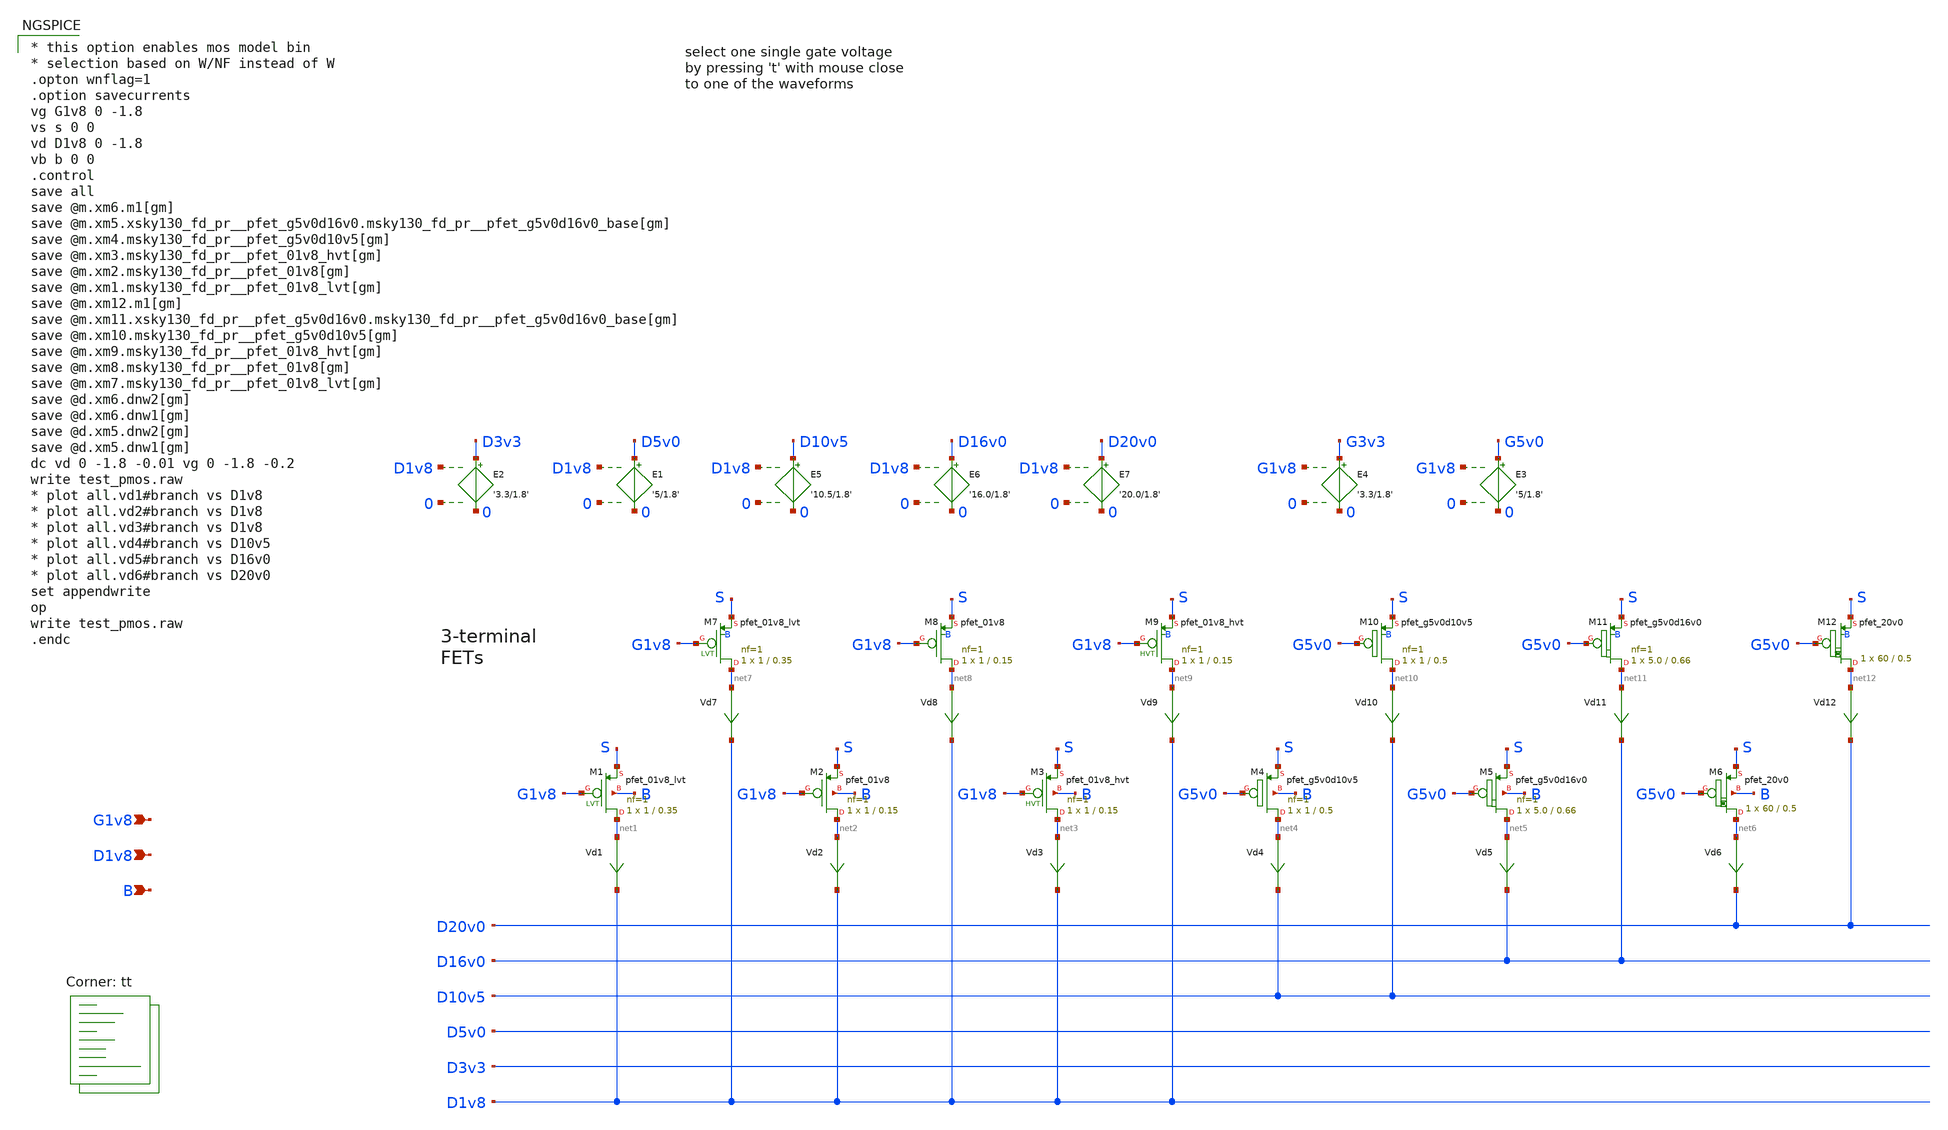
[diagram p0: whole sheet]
** sch_path: sky130A/xschem_libs/sky130_tests/test_pmos/schematic/test_pmos.sch
* Copyright 2021 Stefan Frederik Schippers
* Licensed under the Apache License, Version 2.0 (the "License");
* you may not use this file except in compliance with the License.
* You may obtain a copy of the License at
* https://www.apache.org/licenses/LICENSE-2.0
* Unless required by applicable law or agreed to in writing, software
* distributed under the License is distributed on an "AS IS" BASIS,
* WITHOUT WARRANTIES OR CONDITIONS OF ANY KIND, either express or implied.
* See the License for the specific language governing permissions and
* limitations under the License.
**.subckt test_pmos G1v8 D1v8 B
*.ipin G1v8
*.ipin D1v8
*.ipin B
Vd1 net1 D1v8 0
.save i(vd1)
Vd2 net2 D1v8 0
.save i(vd2)
E1 D5v0 0 D1v8 0 '5/1.8'
E2 D3v3 0 D1v8 0 '3.3/1.8'
E3 G5v0 0 G1v8 0 '5/1.8'
E4 G3v3 0 G1v8 0 '3.3/1.8'
E5 D10v5 0 D1v8 0 '10.5/1.8'
Vd3 net3 D1v8 0
.save i(vd3)
XM3 net3 G1v8 S B sky130_fd_pr__pfet_01v8_hvt L=0.15 W=1 nf=1 ad='int((1 + 1)/2) * 1 / 1 * 0.29' as='int((1 + 2)/2) * 1 / 1 * 0.29'
+ pd='2*int((1 + 1)/2) * (1 / 1 + 0.29)' ps='2*int((1 + 2)/2) * (1 / 1 + 0.29)' nrd='0.29 / 1 ' nrs='0.29 / 1 '
+ sa=0 sb=0 sd=0 mult=1 m=1
Vd4 net4 D10v5 0
.save i(vd4)
XM4 net4 G5v0 S B sky130_fd_pr__pfet_g5v0d10v5 L=0.5 W=1 nf=1 ad='int((1 + 1)/2) * 1 / 1 * 0.29' as='int((1 + 2)/2) * 1 / 1 * 0.29'
+ pd='2*int((1 + 1)/2) * (1 / 1 + 0.29)' ps='2*int((1 + 2)/2) * (1 / 1 + 0.29)' nrd='0.29 / 1 ' nrs='0.29 / 1 '
+ sa=0 sb=0 sd=0 mult=1 m=1
XM1 net1 G1v8 S B sky130_fd_pr__pfet_01v8_lvt L=0.35 W=1 nf=1 ad='int((1 + 1)/2) * 1 / 1 * 0.29' as='int((1 + 2)/2) * 1 / 1 * 0.29'
+ pd='2*int((1 + 1)/2) * (1 / 1 + 0.29)' ps='2*int((1 + 2)/2) * (1 / 1 + 0.29)' nrd='0.29 / 1 ' nrs='0.29 / 1 '
+ sa=0 sb=0 sd=0 mult=1 m=1
XM2 net2 G1v8 S B sky130_fd_pr__pfet_01v8 L=0.15 W=1 nf=1 ad='int((nf+1)/2) * W/nf * 0.29' as='int((nf+2)/2) * W/nf * 0.29'
+ pd='2*int((nf+1)/2) * (W/nf + 0.29)' ps='2*int((nf+2)/2) * (W/nf + 0.29)' nrd='0.29 / W' nrs='0.29 / W'
+ sa=0 sb=0 sd=0 mult=1 m=1
Vd5 net5 D16v0 0
.save i(vd5)
XM5 net5 G5v0 S B sky130_fd_pr__pfet_g5v0d16v0 L=0.66 W=5.0 nf=1 ad='int((nf+1)/2) * W/nf * 0.29' as='int((nf+2)/2) * W/nf * 0.29'
+ pd='2*int((nf+1)/2) * (W/nf + 0.29)' ps='2*int((nf+2)/2) * (W/nf + 0.29)' nrd='0.29 / W' nrs='0.29 / W'
+ sa=0 sb=0 sd=0 mult=1 m=1
E6 D16v0 0 D1v8 0 '16.0/1.8'
E7 D20v0 0 D1v8 0 '20.0/1.8'
XM6 net6 G5v0 S B sky130_fd_pr__pfet_20v0 L=0.5 W=60 m=1
Vd6 net6 D20v0 0
.save i(vd6)
Vd7 net7 D1v8 0
.save i(vd7)
Vd8 net8 D1v8 0
.save i(vd8)
Vd9 net9 D1v8 0
.save i(vd9)
XM9 net9 G1v8 S B sky130_fd_pr__pfet_01v8_hvt L=0.15 W=1 nf=1 ad='int((1 + 1)/2) * 1 / 1 * 0.29' as='int((1 + 2)/2) * 1 / 1 * 0.29'
+ pd='2*int((1 + 1)/2) * (1 / 1 + 0.29)' ps='2*int((1 + 2)/2) * (1 / 1 + 0.29)' nrd='0.29 / 1 ' nrs='0.29 / 1 '
+ sa=0 sb=0 sd=0 mult=1 m=1
Vd10 net10 D10v5 0
.save i(vd10)
XM10 net10 G5v0 S B sky130_fd_pr__pfet_g5v0d10v5 L=0.5 W=1 nf=1 ad='int((nf+1)/2) * W/nf * 0.29' as='int((nf+2)/2) * W/nf * 0.29'
+ pd='2*int((nf+1)/2) * (W/nf + 0.29)' ps='2*int((nf+2)/2) * (W/nf + 0.29)' nrd='0.29 / W' nrs='0.29 / W'
+ sa=0 sb=0 sd=0 mult=1 m=1
XM7 net7 G1v8 S B sky130_fd_pr__pfet_01v8_lvt L=0.35 W=1 nf=1 ad='int((1 + 1)/2) * 1 / 1 * 0.29' as='int((1 + 2)/2) * 1 / 1 * 0.29'
+ pd='2*int((1 + 1)/2) * (1 / 1 + 0.29)' ps='2*int((1 + 2)/2) * (1 / 1 + 0.29)' nrd='0.29 / 1 ' nrs='0.29 / 1 '
+ sa=0 sb=0 sd=0 mult=1 m=1
XM8 net8 G1v8 S B sky130_fd_pr__pfet_01v8 L=0.15 W=1 nf=1 ad='int((1 + 1)/2) * 1 / 1 * 0.29' as='int((1 + 2)/2) * 1 / 1 * 0.29'
+ pd='2*int((1 + 1)/2) * (1 / 1 + 0.29)' ps='2*int((1 + 2)/2) * (1 / 1 + 0.29)' nrd='0.29 / 1 ' nrs='0.29 / 1 '
+ sa=0 sb=0 sd=0 mult=1 m=1
Vd11 net11 D16v0 0
.save i(vd11)
XM11 net11 G5v0 S B sky130_fd_pr__pfet_g5v0d16v0 L=0.66 W=5.0 nf=1 ad='int((1 + 1)/2) * 5.0 / 1 * 0.29'
+ as='int((1 + 2)/2) * 5.0 / 1 * 0.29' pd='2*int((1 + 1)/2) * (5.0 / 1 + 0.29)' ps='2*int((1 + 2)/2) * (5.0 / 1 + 0.29)'
+ nrd='0.29 / 5.0 ' nrs='0.29 / 5.0 ' sa=0 sb=0 sd=0 mult=1 m=1
XM12 net12 G5v0 S B sky130_fd_pr__pfet_20v0 L=0.5 W=60 m=1
Vd12 net12 D20v0 0
.save i(vd12)
**** begin user architecture code

* this option enables mos model bin
* selection based on W/NF instead of W
.opton wnflag=1
.option savecurrents
vg G1v8 0 -1.8
vs s 0 0
vd D1v8 0 -1.8
vb b 0 0
.control
save all
save @m.xm6.m1[gm]
save @m.xm5.xsky130_fd_pr__pfet_g5v0d16v0.msky130_fd_pr__pfet_g5v0d16v0_base[gm]
save @m.xm4.msky130_fd_pr__pfet_g5v0d10v5[gm]
save @m.xm3.msky130_fd_pr__pfet_01v8_hvt[gm]
save @m.xm2.msky130_fd_pr__pfet_01v8[gm]
save @m.xm1.msky130_fd_pr__pfet_01v8_lvt[gm]
save @m.xm12.m1[gm]
save @m.xm11.xsky130_fd_pr__pfet_g5v0d16v0.msky130_fd_pr__pfet_g5v0d16v0_base[gm]
save @m.xm10.msky130_fd_pr__pfet_g5v0d10v5[gm]
save @m.xm9.msky130_fd_pr__pfet_01v8_hvt[gm]
save @m.xm8.msky130_fd_pr__pfet_01v8[gm]
save @m.xm7.msky130_fd_pr__pfet_01v8_lvt[gm]
save @d.xm6.dnw2[gm]
save @d.xm6.dnw1[gm]
save @d.xm5.dnw2[gm]
save @d.xm5.dnw1[gm]
dc vd 0 -1.8 -0.01 vg 0 -1.8 -0.2
write test_pmos.raw
* plot all.vd1#branch vs D1v8
* plot all.vd2#branch vs D1v8
* plot all.vd3#branch vs D1v8
* plot all.vd4#branch vs D10v5
* plot all.vd5#branch vs D16v0
* plot all.vd6#branch vs D20v0
set appendwrite
op
write test_pmos.raw
.endc


.lib $::SKYWATER_MODELS/sky130.lib.spice tt
**** end user architecture code
**.ends
.end
